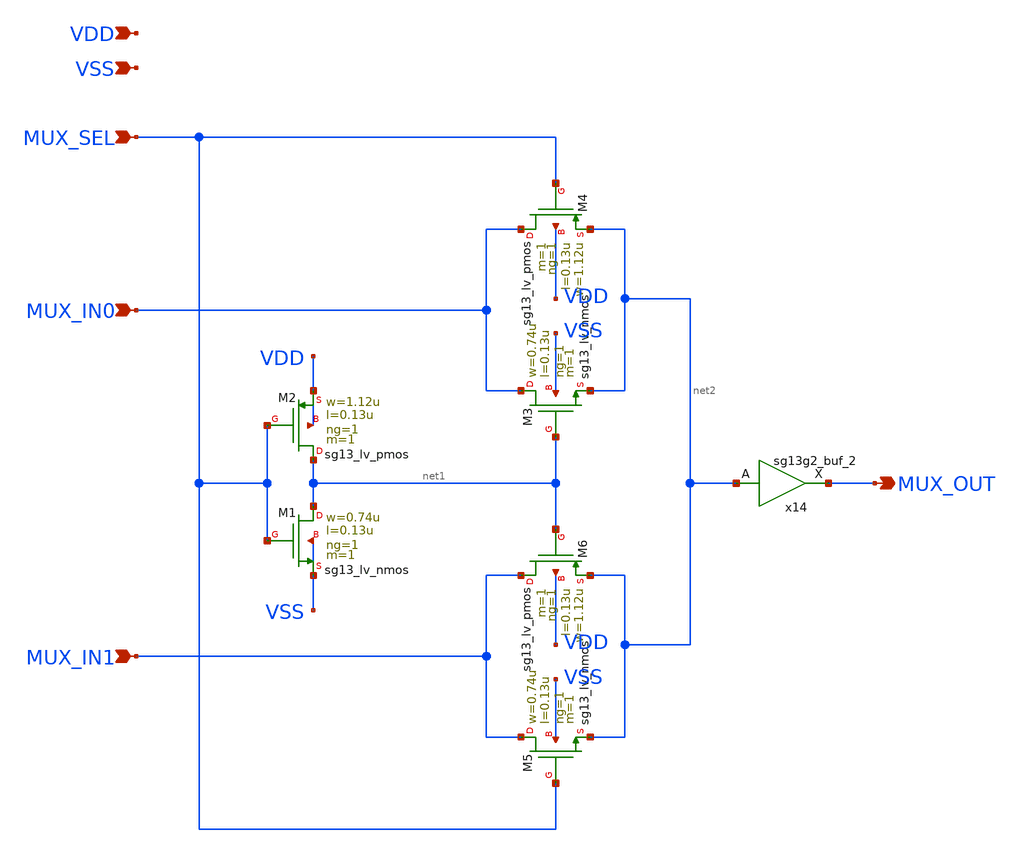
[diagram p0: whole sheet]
** sch_path: schematics/hx_mux_2to1_root.sch
**.subckt hx_mux_2to1_root VDD VSS MUX_IN0 MUX_OUT MUX_IN1 MUX_SEL
*.ipin VDD
*.ipin VSS
*.ipin MUX_IN0
*.opin MUX_OUT
*.ipin MUX_IN1
*.ipin MUX_SEL
XM1 net1 MUX_SEL VSS VSS sg13_lv_nmos w=0.74u l=0.13u ng=1 m=1 mm_ok=1
XM2 net1 MUX_SEL VDD VDD sg13_lv_pmos w=1.12u l=0.13u ng=1 m=1 mm_ok=1
XM3 MUX_IN0 net1 net2 VSS sg13_lv_nmos w=0.74u l=0.13u ng=1 m=1 mm_ok=1
XM4 MUX_IN0 MUX_SEL net2 VDD sg13_lv_pmos w=1.12u l=0.13u ng=1 m=1 mm_ok=1
XM5 MUX_IN1 MUX_SEL net2 VSS sg13_lv_nmos w=0.74u l=0.13u ng=1 m=1 mm_ok=1
XM6 MUX_IN1 net1 net2 VDD sg13_lv_pmos w=1.12u l=0.13u ng=1 m=1 mm_ok=1
x14 MUX_OUT net2 VDD VSS sg13g2_buf_2
**.ends

* expanding   symbol:  sg13g2_buf_2.sym # of pins=2
** sym_path: sg13g2_buf_2.sym
** sch_path: sg13g2_buf_2.sch
.subckt sg13g2_buf_2 X A VDD VSS
*.ipin A
*.opin X
*.iopin VDD
*.iopin VSS
XM1 net1 A VSS VSS sg13_lv_nmos w=640.00n l=130.00n ng=1 m=1 mm_ok=1
XM2 X net1 VSS VSS sg13_lv_nmos w=1.48u l=130.00n ng=2 m=1 mm_ok=1
XM3 net1 A VDD VDD sg13_lv_pmos w=1.000u l=130.00n ng=1 m=1 mm_ok=1
XM4 X net1 VDD VDD sg13_lv_pmos w=2.24u l=130.00n ng=2 m=1 mm_ok=1
.ends

.end
